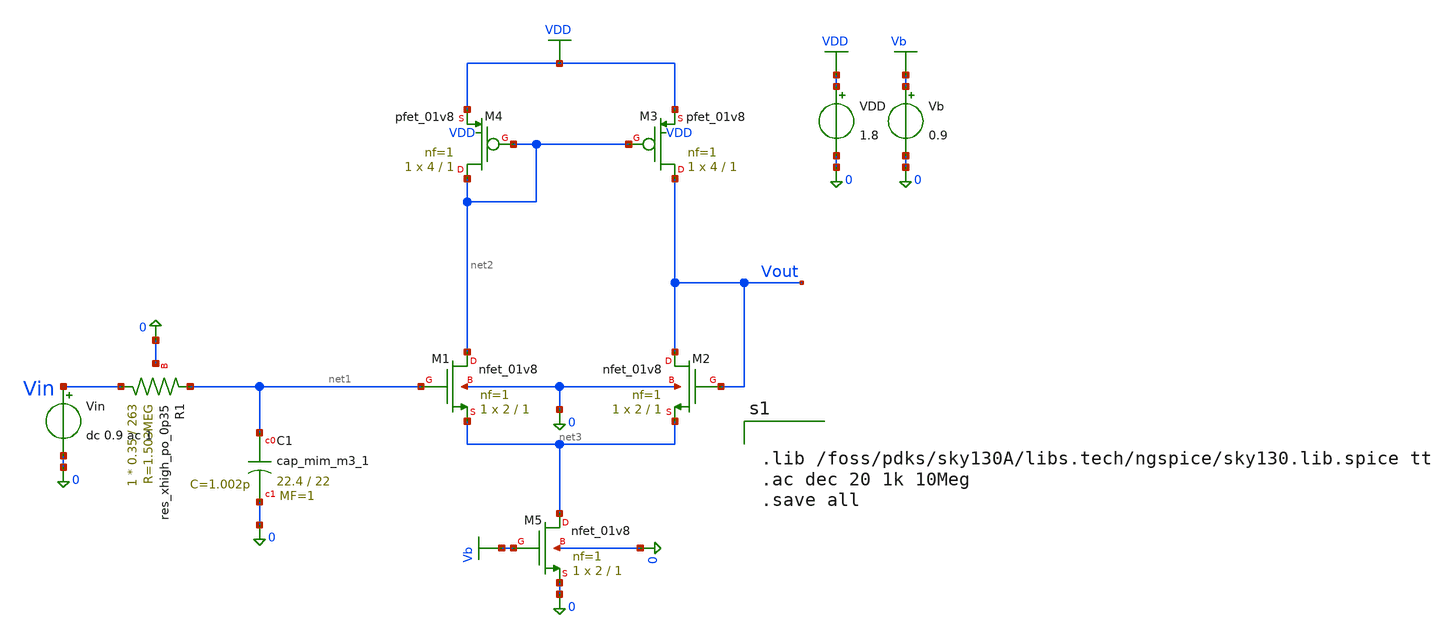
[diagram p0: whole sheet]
** sch_path: LPF.sch
**.subckt LPF
XR1 Vin net1 0 sky130_fd_pr__res_xhigh_po_0p35 L=263 mult=1 m=1
XC1 net1 0 sky130_fd_pr__cap_mim_m3_1 W=22.4 L=22 MF=1 m=1
XM1 net2 net1 net3 0 sky130_fd_pr__nfet_01v8 L=1 W=2 nf=1 ad='int((1 + 1)/2) * 2 / 1 * 0.29' as='int((1 + 2)/2) * 2 / 1 * 0.29'
+ pd='2*int((1 + 1)/2) * (2 / 1 + 0.29)' ps='2*int((1 + 2)/2) * (2 / 1 + 0.29)' nrd='0.29 / 2 ' nrs='0.29 / 2 '
+ sa=0 sb=0 sd=0 mult=1 m=1
XM2 Vout Vout net3 0 sky130_fd_pr__nfet_01v8 L=1 W=2 nf=1 ad='int((1 + 1)/2) * 2 / 1 * 0.29' as='int((1 + 2)/2) * 2 / 1 * 0.29'
+ pd='2*int((1 + 1)/2) * (2 / 1 + 0.29)' ps='2*int((1 + 2)/2) * (2 / 1 + 0.29)' nrd='0.29 / 2 ' nrs='0.29 / 2 '
+ sa=0 sb=0 sd=0 mult=1 m=1
XM5 net3 Vb 0 0 sky130_fd_pr__nfet_01v8 L=1 W=2 nf=1 ad='int((1 + 1)/2) * 2 / 1 * 0.29' as='int((1 + 2)/2) * 2 / 1 * 0.29'
+ pd='2*int((1 + 1)/2) * (2 / 1 + 0.29)' ps='2*int((1 + 2)/2) * (2 / 1 + 0.29)' nrd='0.29 / 2 ' nrs='0.29 / 2 '
+ sa=0 sb=0 sd=0 mult=1 m=1
XM3 Vout net2 VDD VDD sky130_fd_pr__pfet_01v8 L=1 W=4 nf=1 ad='int((1 + 1)/2) * 4 / 1 * 0.29' as='int((1 + 2)/2) * 4 / 1 * 0.29'
+ pd='2*int((1 + 1)/2) * (4 / 1 + 0.29)' ps='2*int((1 + 2)/2) * (4 / 1 + 0.29)' nrd='0.29 / 4 ' nrs='0.29 / 4 '
+ sa=0 sb=0 sd=0 mult=1 m=1
XM4 net2 net2 VDD VDD sky130_fd_pr__pfet_01v8 L=1 W=4 nf=1 ad='int((1 + 1)/2) * 4 / 1 * 0.29' as='int((1 + 2)/2) * 4 / 1 * 0.29'
+ pd='2*int((1 + 1)/2) * (4 / 1 + 0.29)' ps='2*int((1 + 2)/2) * (4 / 1 + 0.29)' nrd='0.29 / 4 ' nrs='0.29 / 4 '
+ sa=0 sb=0 sd=0 mult=1 m=1
VDD VDD 0 1.8
Vb Vb 0 0.9
Vin Vin 0 dc 0.9 ac 1
**** begin user architecture code


.lib /foss/pdks/sky130A/libs.tech/ngspice/sky130.lib.spice tt
.ac dec 20 1k 10Meg
.save all


**** end user architecture code
**.ends
.GLOBAL VDD
.GLOBAL Vb
.end
